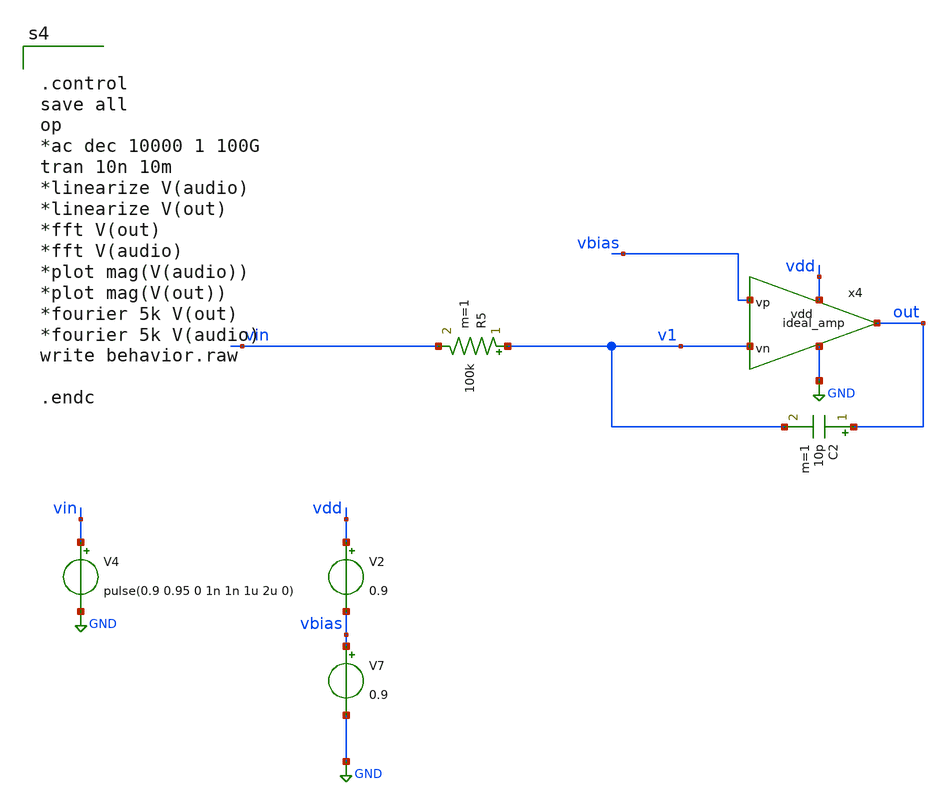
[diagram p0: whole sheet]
** sch_path: xschem/src/behavior_mdl/OTA_test.sch
**.subckt OTA_test
V2 vdd vbias 0.9
V4 vin GND pulse(0.9 0.95 0 1n 1n 1u 2u 0)
R5 v1 vin 100k m=1
C2 out v1 10p m=1
x4 vbias v1 out vdd GND ideal_amp
V7 vbias GND 0.9
**** begin user architecture code


.include /home/eda/xschem/xschem_library/src/behavior_mdl/comparator.spice
.include /home/eda/xschem/xschem_library/src/behavior_mdl/switch.spice
.include /home/eda/xschem/xschem_library/src/behavior_mdl/integrator_feedback.spice
.include /home/eda/xschem/xschem_library/src/behavior_mdl/integrator_input.spice
.include /home/eda/xschem/xschem_library/src/behavior_mdl/adder.spice
.include /home/eda/xschem/xschem_library/src/behavior_mdl/triang.spice
.include /home/eda/xschem/xschem_library/src/behavior_mdl/ideal_amp.spice
.include /home/eda/xschem/xschem_library/src/behavior_mdl/limiter.spice




.control
save all
op
*ac dec 10000 1 100G
tran 10n 10m
*linearize V(audio)
*linearize V(out)
*fft V(out)
*fft V(audio)
*plot mag(V(audio))
*plot mag(V(out))
*fourier 5k V(out)
*fourier 5k V(audio)
write behavior.raw

.endc





.include /home/eda/pdk/skywater-pdk/libraries/sky130_fd_pr_ngspice/latest/models/corners/tt.spice


* Resistor$::SKYWATER_MODELS/Capacitor
.include $::SKYWATER_MODELS/models/r+c/res_typical__cap_typical.spice
.include $::SKYWATER_MODELS/models/r+c/res_typical__cap_typical__lin.spice
* Special cells
.include $::SKYWATER_MODELS/models/corners/tt/specialized_cells.spice


**** end user architecture code
**.ends
.GLOBAL GND
.end
